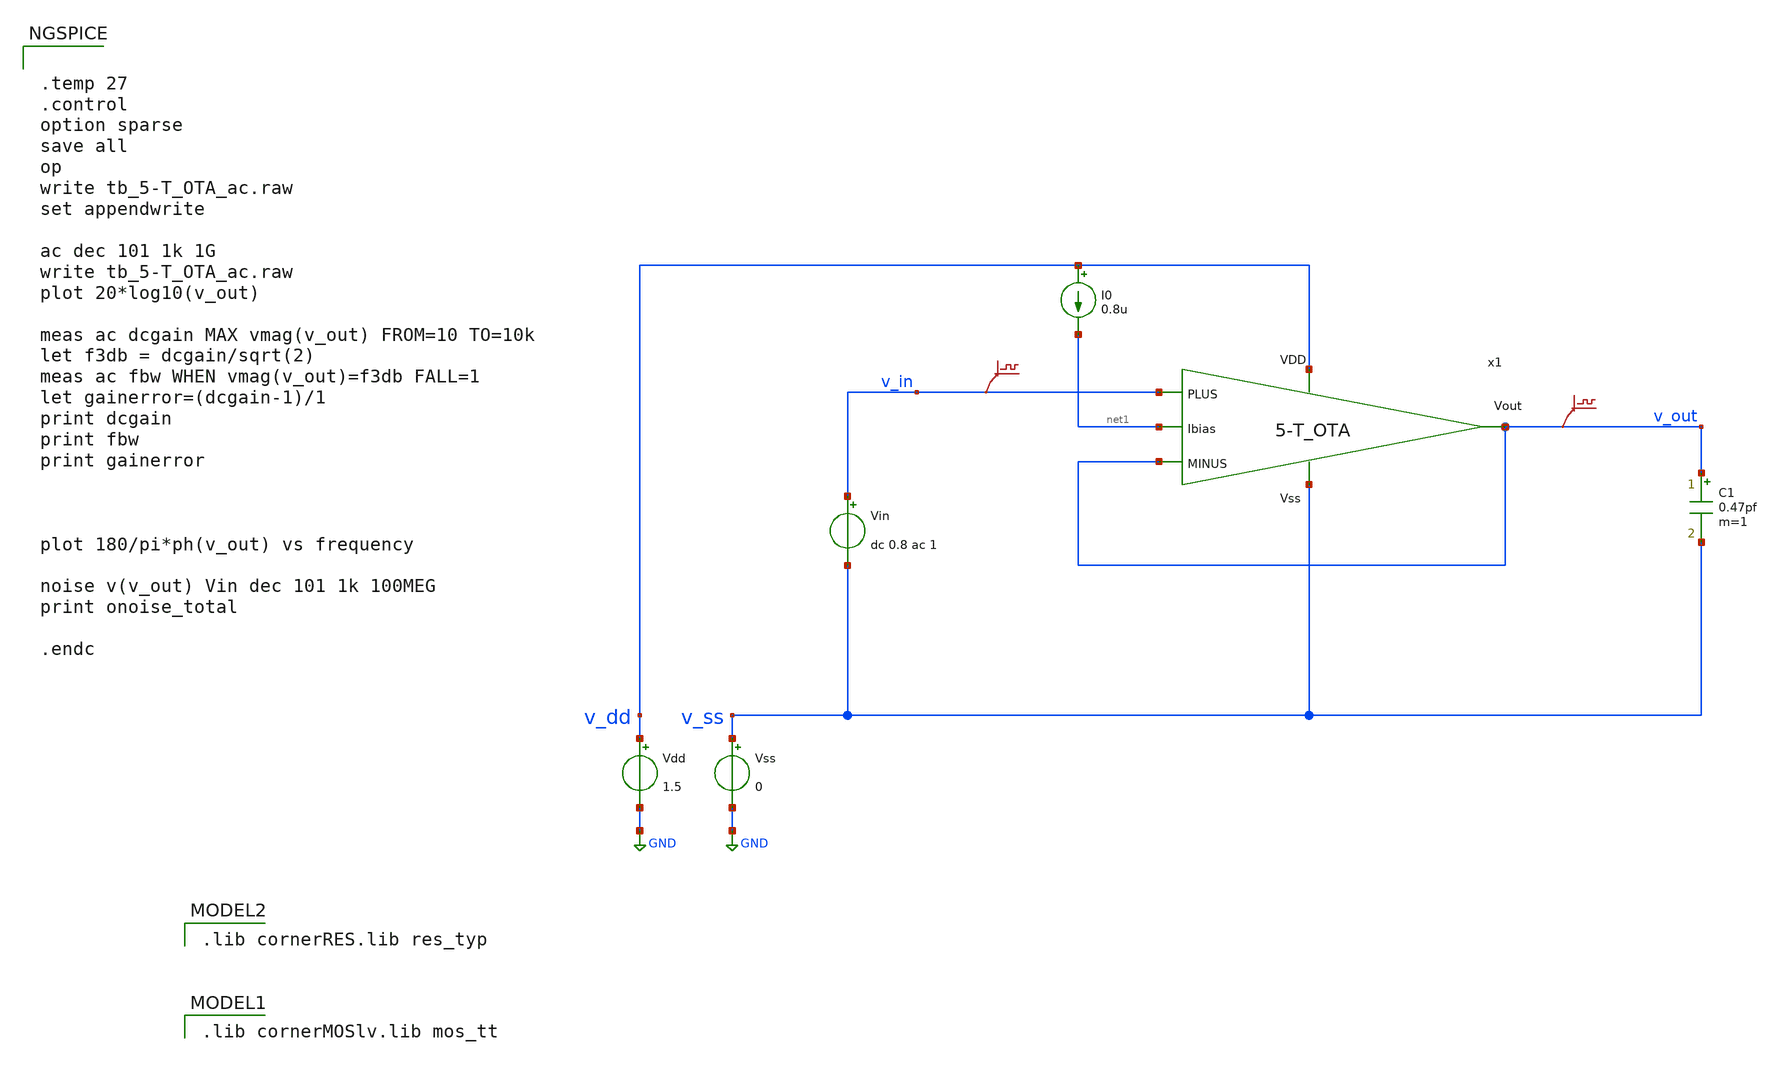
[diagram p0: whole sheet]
** sch_path: DSM/Schematics/Designs_Hrishi/RealCircuits/5-T_OTA/tb_5-T_OTA_ac.sch
* (c) 2024 Hrishikesh, @HSB
**.subckt tb_5-T_OTA_ac
Vdd v_dd GND 1.5
Vss v_ss GND 0
C1 v_out v_ss 0.47pf m=1
Vin v_in v_ss dc 0.8 ac 1
I0 v_dd net1 0.8u
.save v(v_in)
.save v(v_out)
x1 v_dd net1 v_out v_in v_out v_ss 5-T_OTA
**** begin user architecture code
 .lib cornerMOSlv.lib mos_tt

 .lib cornerRES.lib res_typ



.temp 27
.control
option sparse
save all
op
write tb_5-T_OTA_ac.raw
set appendwrite

ac dec 101 1k 1G
write tb_5-T_OTA_ac.raw
plot 20*log10(v_out)

meas ac dcgain MAX vmag(v_out) FROM=10 TO=10k
let f3db = dcgain/sqrt(2)
meas ac fbw WHEN vmag(v_out)=f3db FALL=1
let gainerror=(dcgain-1)/1
print dcgain
print fbw
print gainerror



plot 180/pi*ph(v_out) vs frequency

noise v(v_out) Vin dec 101 1k 100MEG
print onoise_total

.endc


**** end user architecture code
**.ends

* expanding   symbol:
*+  /foss/designs/CEMS_DSM/DSM/Schematics/IC_Designs_Hrishi/RealCircuits/5-T_OTA/5-T_OTA.sym # of pins=6
** sym_path: DSM/Schematics/Designs_Hrishi/RealCircuits/5-T_OTA/5-T_OTA.sym
** sch_path: DSM/Schematics/Designs_Hrishi/RealCircuits/5-T_OTA/5-T_OTA.sch
.subckt 5-T_OTA VDD Ibias Vout PLUS MINUS Vss
*.ipin MINUS
*.ipin PLUS
*.ipin VDD
*.ipin Ibias
*.ipin Vss
*.opin Vout
XM10 Vout net1 VDD VDD sg13_lv_pmos w=0.136u l=0.5u ng=1 m=1 mm_ok=1
XM11 net1 net1 VDD VDD sg13_lv_pmos w=0.136u l=0.5u ng=1 m=1 mm_ok=1
XM12 net1 PLUS net2 Vss sg13_lv_nmos w=0.15u l=2u ng=1 m=1 mm_ok=1
XM13 Vout MINUS net2 Vss sg13_lv_nmos w=0.15u l=2u ng=1 m=1 mm_ok=1
XM14 net2 net4 Vss Vss sg13_lv_nmos w=0.30u l=2u ng=1 m=1 mm_ok=1
XM1 net3 net4 Vss Vss sg13_lv_nmos w=0.15u l=2u ng=1 m=1 mm_ok=1
XM2 VDD VDD net3 Vss sg13_lv_nmos w=0.15u l=2u ng=1 m=1 mm_ok=1
XM3 net4 net4 Vss Vss sg13_lv_nmos w=0.15u l=2u ng=1 m=1 mm_ok=1
XM4 Ibias VDD net4 Vss sg13_lv_nmos w=0.15u l=2u ng=1 m=1 mm_ok=1
.ends

.GLOBAL GND
.end
